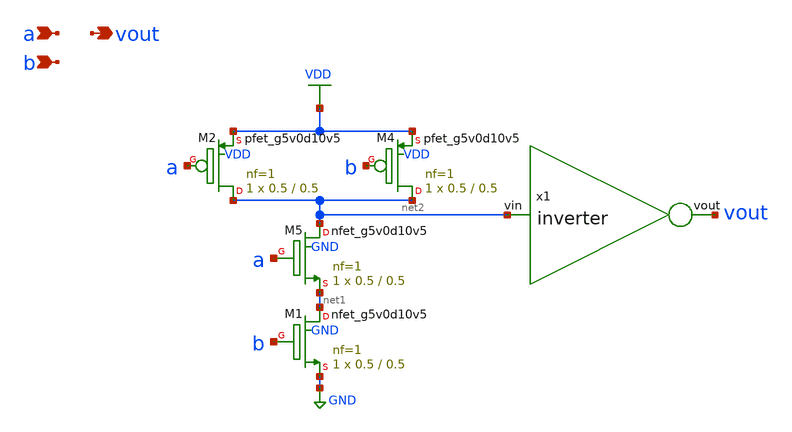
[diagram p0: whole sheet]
** sch_path: schematics/and.sch
**.subckt and a vout b
*.ipin a
*.opin vout
*.ipin b
XM1 net1 b GND GND sky130_fd_pr__nfet_g5v0d10v5 L=0.5 W=0.5 nf=1 ad='int((nf+1)/2) * W/nf * 0.29' as='int((nf+2)/2) * W/nf * 0.29'
+ pd='2*int((nf+1)/2) * (W/nf + 0.29)' ps='2*int((nf+2)/2) * (W/nf + 0.29)' nrd='0.29 / W' nrs='0.29 / W'
+ sa=0 sb=0 sd=0 mult=1 m=1
XM5 net2 a net1 GND sky130_fd_pr__nfet_g5v0d10v5 L=0.5 W=0.5 nf=1 ad='int((nf+1)/2) * W/nf * 0.29' as='int((nf+2)/2) * W/nf * 0.29'
+ pd='2*int((nf+1)/2) * (W/nf + 0.29)' ps='2*int((nf+2)/2) * (W/nf + 0.29)' nrd='0.29 / W' nrs='0.29 / W'
+ sa=0 sb=0 sd=0 mult=1 m=1
XM2 net2 a VDD VDD sky130_fd_pr__pfet_g5v0d10v5 L=0.5 W=0.5 nf=1 ad='int((nf+1)/2) * W/nf * 0.29' as='int((nf+2)/2) * W/nf * 0.29'
+ pd='2*int((nf+1)/2) * (W/nf + 0.29)' ps='2*int((nf+2)/2) * (W/nf + 0.29)' nrd='0.29 / W' nrs='0.29 / W'
+ sa=0 sb=0 sd=0 mult=1 m=1
XM4 net2 b VDD VDD sky130_fd_pr__pfet_g5v0d10v5 L=0.5 W=0.5 nf=1 ad='int((nf+1)/2) * W/nf * 0.29' as='int((nf+2)/2) * W/nf * 0.29'
+ pd='2*int((nf+1)/2) * (W/nf + 0.29)' ps='2*int((nf+2)/2) * (W/nf + 0.29)' nrd='0.29 / W' nrs='0.29 / W'
+ sa=0 sb=0 sd=0 mult=1 m=1
x1 vout net2 inverter
**.ends

* expanding   symbol:  /media/sf_share/final_project/inverter.sym # of pins=2
** sym_path: schematics/inverter.sym
** sch_path: schematics/inverter.sch
.subckt inverter vout vin
*.ipin vin
*.opin vout
XM3 vout vin VDD VDD sky130_fd_pr__pfet_g5v0d10v5 L=0.5 W=0.5 nf=1 ad='int((nf+1)/2) * W/nf * 0.29' as='int((nf+2)/2) * W/nf * 0.29'
+ pd='2*int((nf+1)/2) * (W/nf + 0.29)' ps='2*int((nf+2)/2) * (W/nf + 0.29)' nrd='0.29 / W' nrs='0.29 / W'
+ sa=0 sb=0 sd=0 mult=1 m=1
XM5 vout vin GND GND sky130_fd_pr__nfet_g5v0d10v5 L=0.5 W=0.5 nf=1 ad='int((nf+1)/2) * W/nf * 0.29' as='int((nf+2)/2) * W/nf * 0.29'
+ pd='2*int((nf+1)/2) * (W/nf + 0.29)' ps='2*int((nf+2)/2) * (W/nf + 0.29)' nrd='0.29 / W' nrs='0.29 / W'
+ sa=0 sb=0 sd=0 mult=1 m=1
.ends

.GLOBAL GND
.GLOBAL VDD
.end
